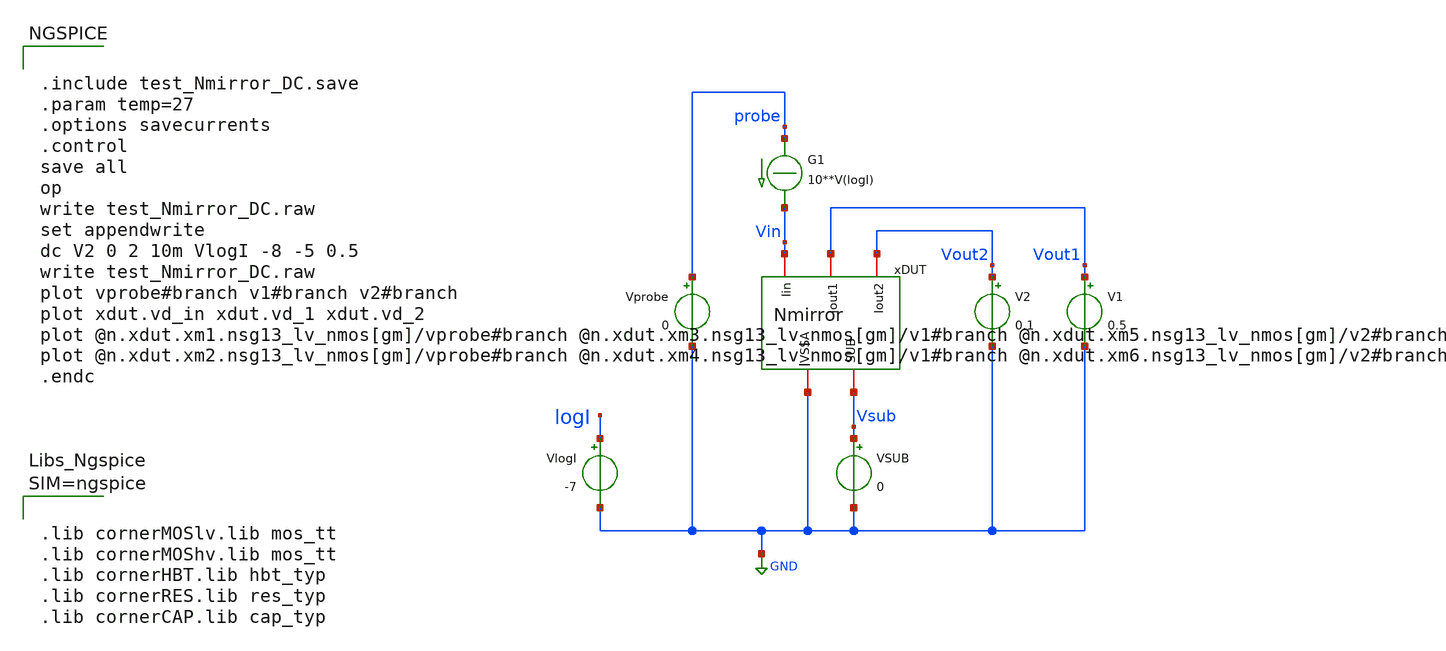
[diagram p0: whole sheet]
** sch_path: xschem/test_Nmirror_DC.sch
**.subckt test_Nmirror_DC
xDUT Vout2 Vin Vout1 GND Vsub Nmirror
V1 Vout1 GND 0.5
.save i(v1)
V2 Vout2 GND 0.1
.save i(v2)
VSUB Vsub GND 0
.save i(vsub)
Vprobe probe GND 0
.save i(vprobe)
G1 probe Vin CUR=' 10**V(logI) '
VlogI logI GND -7
.save i(vlogi)
**** begin user architecture code


.include test_Nmirror_DC.save
.param temp=27
.options savecurrents
.control
save all
op
write test_Nmirror_DC.raw
set appendwrite
dc V2 0 2 10m VlogI -8 -5 0.5
write test_Nmirror_DC.raw
plot vprobe#branch v1#branch v2#branch
plot xdut.vd_in xdut.vd_1 xdut.vd_2
plot @n.xdut.xm1.nsg13_lv_nmos[gm]/vprobe#branch @n.xdut.xm3.nsg13_lv_nmos[gm]/v1#branch
+ @n.xdut.xm5.nsg13_lv_nmos[gm]/v2#branch
plot @n.xdut.xm2.nsg13_lv_nmos[gm]/vprobe#branch @n.xdut.xm4.nsg13_lv_nmos[gm]/v1#branch
+ @n.xdut.xm6.nsg13_lv_nmos[gm]/v2#branch
.endc





.lib cornerMOSlv.lib mos_tt
.lib cornerMOShv.lib mos_tt
.lib cornerHBT.lib hbt_typ
.lib cornerRES.lib res_typ
.lib cornerCAP.lib cap_typ



**** end user architecture code
**.ends

* expanding   symbol:  Nmirror.sym # of pins=5
** sym_path: Nmirror.sym
** sch_path: Nmirror.sch
.subckt Nmirror Iout2 Iin Iout1 VSSA SUB
*.iopin VSSA
*.iopin SUB
*.iopin Iin
*.iopin Iout1
*.iopin Iout2
XM1 net3 Iin VSSA SUB sg13_lv_nmos w=1.0u l=4.0u ng=1 m=1 mm_ok=1
XM3 net2 Iin VSSA SUB sg13_lv_nmos w=1.0u l=4.0u ng=1 m=1 mm_ok=1
XM2 Iin Iin net3 SUB sg13_lv_nmos w=1.0u l=0.26u ng=1 m=1 mm_ok=1
XM4 Iout1 Iin net2 SUB sg13_lv_nmos w=1.0u l=0.26u ng=1 m=1 mm_ok=1
XM5 net1 Iin VSSA SUB sg13_lv_nmos w=1.0u l=4.0u ng=1 m=1 mm_ok=1
XM6 Iout2 Iin net1 SUB sg13_lv_nmos w=1.0u l=0.26u ng=1 m=1 mm_ok=1
.ends

.GLOBAL GND
.end
